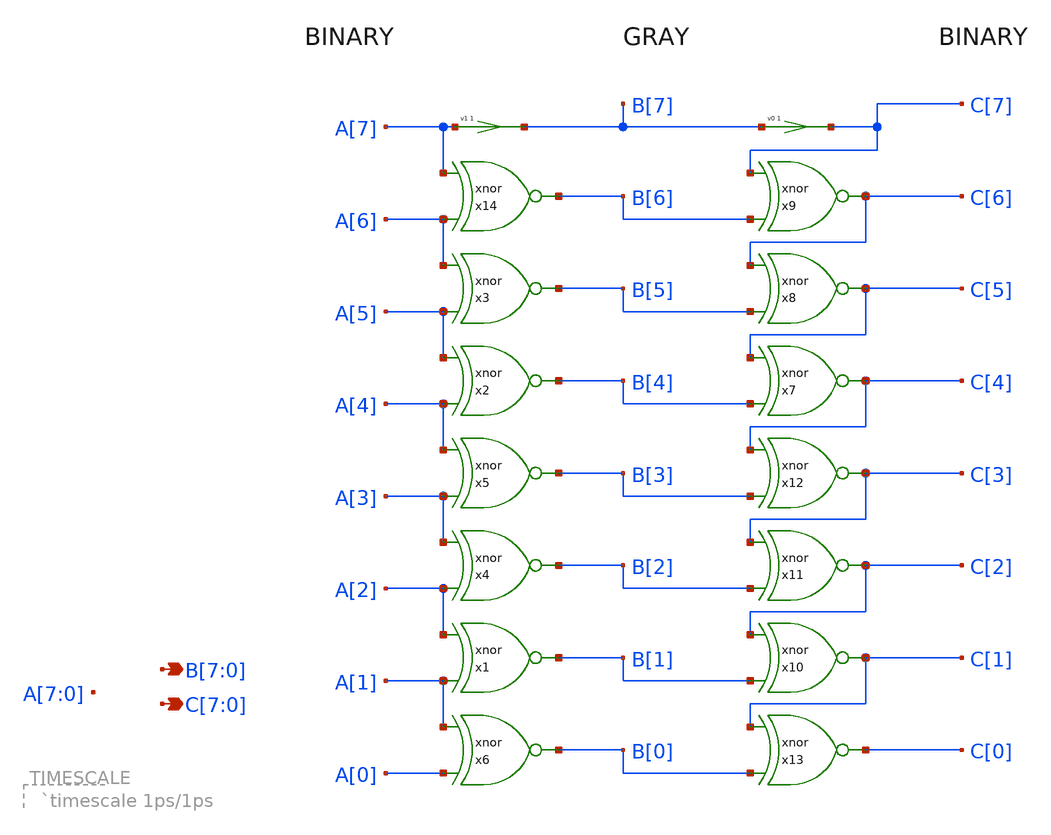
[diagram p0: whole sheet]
** sch_path: xschem_library/examples/greycnt.sch
**.subckt greycnt B[7],B[6],B[5],B[4],B[3],B[2],B[1],B[0] C[7],C[6],C[5],C[4],C[3],C[2],C[1],C[0]
*.opin B[7],B[6],B[5],B[4],B[3],B[2],B[1],B[0]
*.opin C[7],C[6],C[5],C[4],C[3],C[2],C[1],C[0]
v1 B[7] A[7] 0
v0 C[7] B[7] 0
**** begin user architecture code

initial begin
  $dumpfile("dumpfile.vcd");
  $dumpvars;
  A=0;
end

always begin
  #1000;
  $display("%08b %08b", A, B);
  A=A + 1;
  if(A==0) $finish;
end


**** end user architecture code
**.ends
.end
